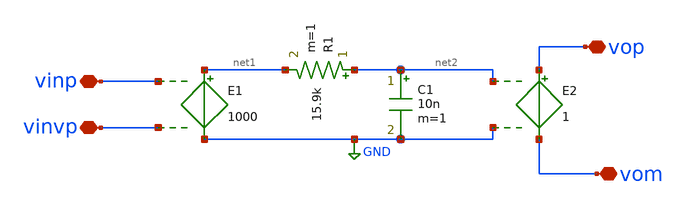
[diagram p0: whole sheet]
** sch_path: highpassop.sch
**.subckt highpassop vinp vinvp vop vom
*.iopin vinp
*.iopin vinvp
*.iopin vop
*.iopin vom
E1 net1 GND vinp vinvp 1000
E2 vop vom net2 GND 1
R1 net2 net1 15.9k m=1
C1 net2 GND 10n m=1
**.ends
.GLOBAL GND
.end
